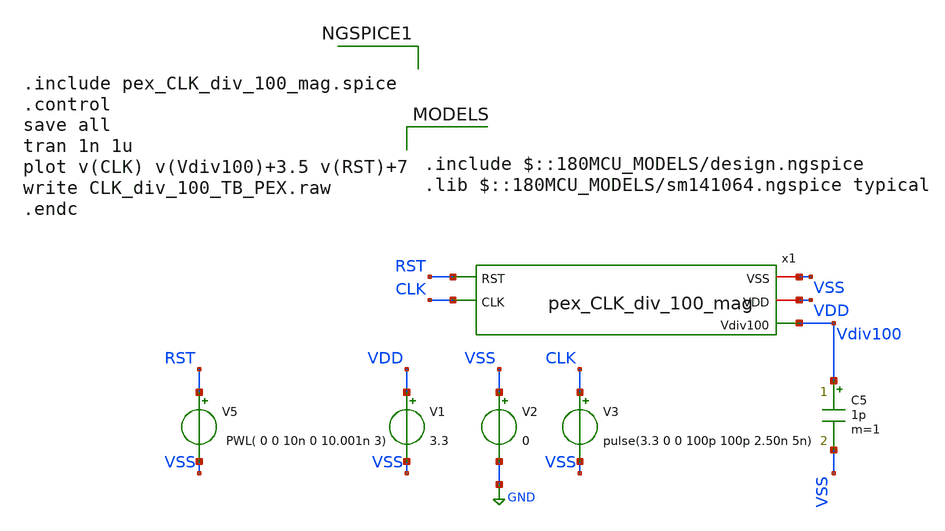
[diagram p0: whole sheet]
** sch_path: Clock_Generator_PAKISTAN_02/Schematics/CLK_div_100_TB_PEX.sch
**.subckt CLK_div_100_TB_PEX
V1 VDD VSS 3.3
V2 VSS GND 0
V3 CLK VSS pulse(3.3 0 0 100p 100p 2.50n 5n)
C5 Vdiv100 VSS 1p m=1
V5 RST VSS PWL( 0 0 10n 0 10.001n 3)
x1 VSS VDD RST Vdiv100 CLK pex_CLK_div_100_mag
**** begin user architecture code

.include $::180MCU_MODELS/design.ngspice
.lib $::180MCU_MODELS/sm141064.ngspice typical



.include pex_CLK_div_100_mag.spice
.control
save all
tran 1n 1u
plot v(CLK) v(Vdiv100)+3.5 v(RST)+7
write CLK_div_100_TB_PEX.raw
.endc


**** end user architecture code
**.ends
.GLOBAL GND
.end
